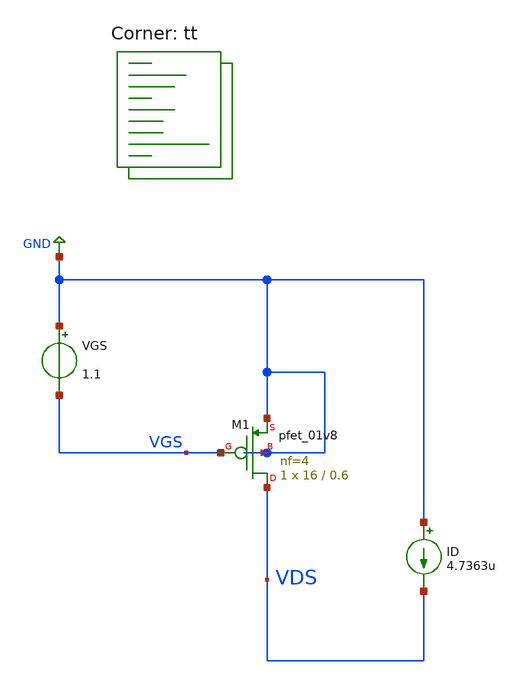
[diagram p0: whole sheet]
** sch_path: projects/bandgapref/xschem_ngspice/new_files/vgs_id_sweep_pfet.sch
**.subckt vgs_id_sweep_pfet
VGS GND VGS 1.1
ID GND VDS 4.7363u
XM1 VDS VGS GND GND sky130_fd_pr__pfet_01v8 L=0.6 W=16 nf=4 ad='int((nf+1)/2) * W/nf * 0.29' as='int((nf+2)/2) * W/nf * 0.29'
+ pd='2*int((nf+1)/2) * (W/nf + 0.29)' ps='2*int((nf+2)/2) * (W/nf + 0.29)' nrd='0.29 / W' nrs='0.29 / W'
+ sa=0 sb=0 sd=0 mult=1 m=1
**** begin user architecture code
.lib $::SKYWATER_MODELS/sky130.lib.spice tt



.option method=gear
.option wnflag=1
.option savecurrents

.save @m.xm1.msky130_fd_pr__pfet_01v8[gm]

.control
  save all
  *  dc VGS 0 1.8 0.1 VDS 0 1.8 0.1
  dc ID 0 20u 0.1u VGS 0 1.8 0.1
  remzerovec
  write vgs_id_sweep_pfet.raw
  set appendwrite
.endc



**** end user architecture code
**.ends
.GLOBAL GND
.end
